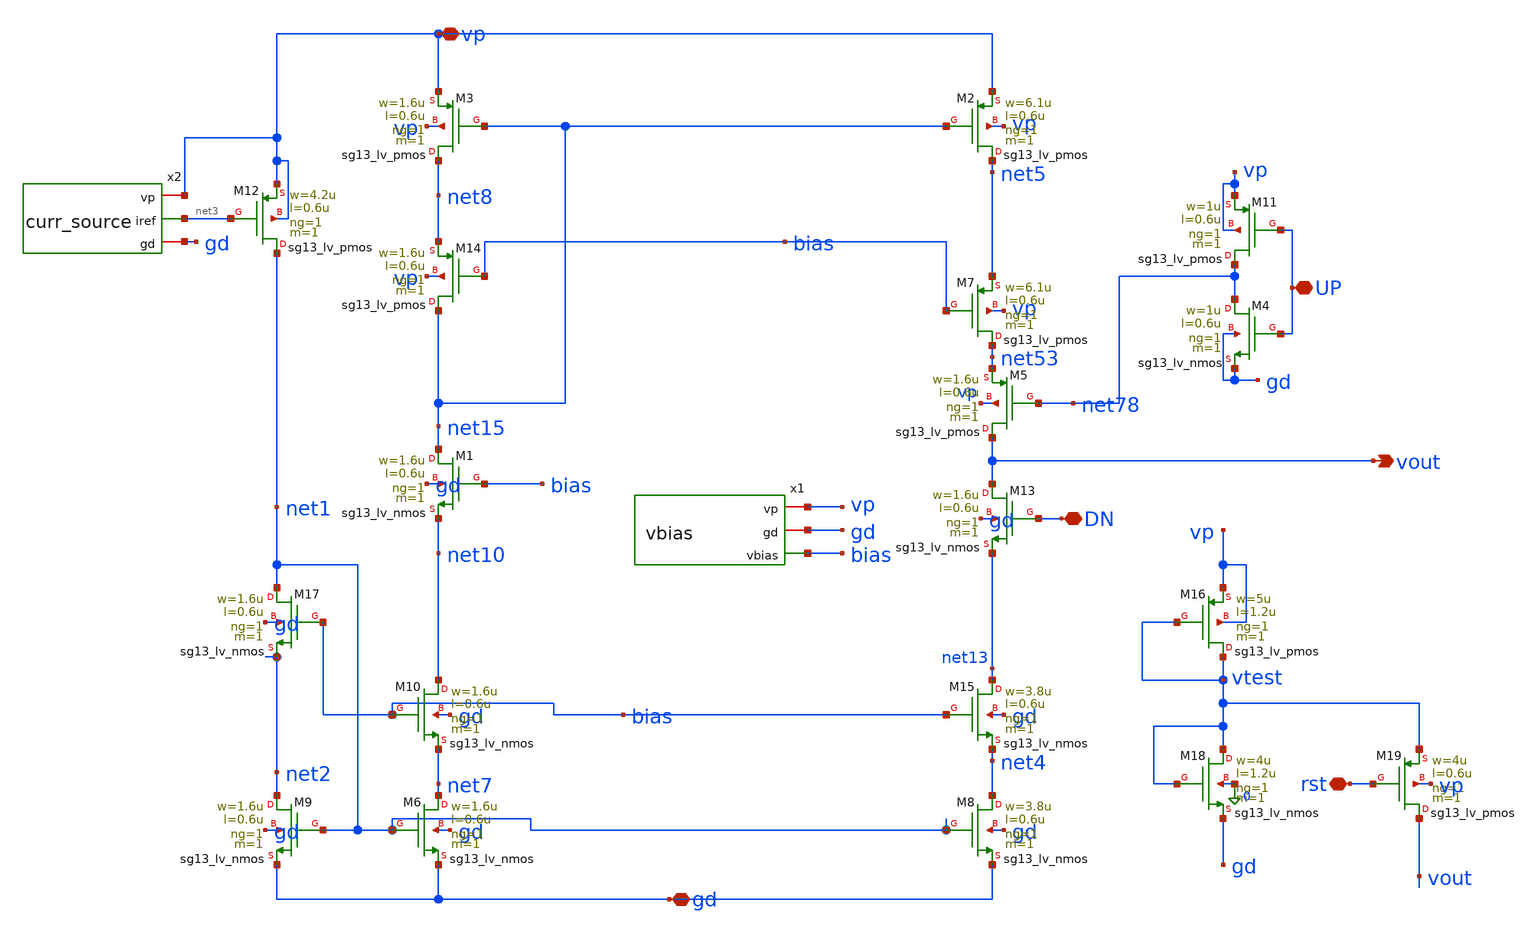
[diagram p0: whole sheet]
** sch_path: PLL0663-main/schematic/xschem/charge_pump/charge_pump_cell_10u.sch
**.subckt charge_pump_cell_10u UP DN gd vp vout rst
*.iopin UP
*.iopin DN
*.iopin gd
*.iopin vp
*.opin vout
*.iopin rst
XM12 net1 net3 vp vp sg13_lv_pmos w=4.2u l=0.6u ng=1 m=1 mm_ok=1
XM3 net8 net15 vp vp sg13_lv_pmos w=1.6u l=0.6u ng=1 m=1 mm_ok=1
XM2 net5 net15 vp vp sg13_lv_pmos w=6.1u l=0.6u ng=1 m=1 mm_ok=1
XM7 net53 bias net5 vp sg13_lv_pmos w=6.1u l=0.6u ng=1 m=1 mm_ok=1
XM11 net78 UP vp vp sg13_lv_pmos w=1u l=0.6u ng=1 m=1 mm_ok=1
XM4 net78 UP gd gd sg13_lv_nmos w=1u l=0.6u ng=1 m=1 mm_ok=1
XM5 vout net78 net53 vp sg13_lv_pmos w=1.6u l=0.6u ng=1 m=1 mm_ok=1
XM13 vout DN net13 gd sg13_lv_nmos w=1.6u l=0.6u ng=1 m=1 mm_ok=1
XM14 net15 bias net8 vp sg13_lv_pmos w=1.6u l=0.6u ng=1 m=1 mm_ok=1
XM1 net15 bias net10 gd sg13_lv_nmos w=1.6u l=0.6u ng=1 m=1 mm_ok=1
XM17 net1 bias net2 gd sg13_lv_nmos w=1.6u l=0.6u ng=1 m=1 mm_ok=1
XM9 net2 net1 gd gd sg13_lv_nmos w=1.6u l=0.6u ng=1 m=1 mm_ok=1
XM10 net10 bias net7 gd sg13_lv_nmos w=1.6u l=0.6u ng=1 m=1 mm_ok=1
XM6 net7 net1 gd gd sg13_lv_nmos w=1.6u l=0.6u ng=1 m=1 mm_ok=1
XM8 net4 net1 gd gd sg13_lv_nmos w=3.8u l=0.6u ng=1 m=1 mm_ok=1
XM15 net13 bias net4 gd sg13_lv_nmos w=3.8u l=0.6u ng=1 m=1 mm_ok=1
XM16 vtest vtest vp vp sg13_lv_pmos w=5u l=1.2u ng=1 m=1 mm_ok=1
XM18 vtest vtest gd 0 sg13_lv_nmos w=4u l=1.2u ng=1 m=1 mm_ok=1
XM19 vout rst vtest vp sg13_lv_pmos w=4u l=0.6u ng=1 m=1 mm_ok=1
x1 vp gd bias vbias
x2 vp net3 gd curr_source
**.ends

* expanding   symbol:
*+  /foss/designs/IHP__PLL0663/PLL0663-main/schematic/xschem/charge_pump/vbias.sym # of pins=3
** sym_path: /foss/designs/IHP__PLL0663/PLL0663-main/schematic/xschem/charge_pump/vbias.sym
** sch_path: /foss/designs/IHP__PLL0663/PLL0663-main/schematic/xschem/charge_pump/vbias.sch
.subckt vbias vp gd vbias
*.opin vbias
*.iopin gd
*.iopin vp
XM5 net1 iref vp vp sg13_lv_pmos w=1.2u l=0.6u ng=1 m=1 mm_ok=1
XM6 vbias net1 net2 gd sg13_lv_nmos w=3.6u l=0.6u ng=1 m=1 mm_ok=1
XM2 net2 net2 gd gd sg13_lv_nmos w=1.2u l=0.6u ng=1 m=1 mm_ok=1
XM3 gd gd gd gd sg13_lv_nmos w=1.86u l=0.6u ng=1 m=1 mm_ok=1
XM7 vp vp vp vp sg13_lv_pmos w=1.375u l=0.6u ng=1 m=1 mm_ok=1
XR1 net1 vbias gd rppd w=1e-6 l=1.7e-6 m=1 b=0 mm_ok=1
x1 vp iref gd curr_source
.ends


* expanding   symbol:
*+  /foss/designs/IHP__PLL0663/PLL0663-main/schematic/xschem/charge_pump/curr_source.sym # of pins=3
** sym_path: /foss/designs/IHP__PLL0663/PLL0663-main/schematic/xschem/charge_pump/curr_source.sym
** sch_path: /foss/designs/IHP__PLL0663/PLL0663-main/schematic/xschem/charge_pump/curr_source.sch
.subckt curr_source vp iref gd
*.iopin vp
*.iopin gd
*.opin iref
XM9 net3 net3 gd gd sg13_lv_nmos w=1u l=0.6u ng=1 m=1 mm_ok=1
XM4 iref iref vp vp sg13_lv_pmos w=1.4u l=0.6u ng=1 m=1 mm_ok=1
XM5 net2 iref vp vp sg13_lv_pmos w=1.2u l=0.6u ng=1 m=1 mm_ok=1
XM10 iref net2 net1 gd sg13_lv_nmos w=1.2u l=0.6u ng=1 m=1 mm_ok=1
XM1 net2 net2 gd gd sg13_lv_nmos w=1.4u l=0.6u ng=1 m=1 mm_ok=1
XM3 vp vp net3 gd sg13_lv_nmos w=1u l=0.6u ng=1 m=1 mm_ok=1
XM6 vp net3 iref gd sg13_lv_nmos w=1u l=0.6u ng=1 m=1 mm_ok=1
XM2 gd gd gd gd sg13_lv_nmos w=0.4u l=0.6u ng=1 m=1 mm_ok=1
XR2 net1 gd gd rppd w=1e-6 l=1.7e-6 m=1 b=0 mm_ok=1
.ends

.end
